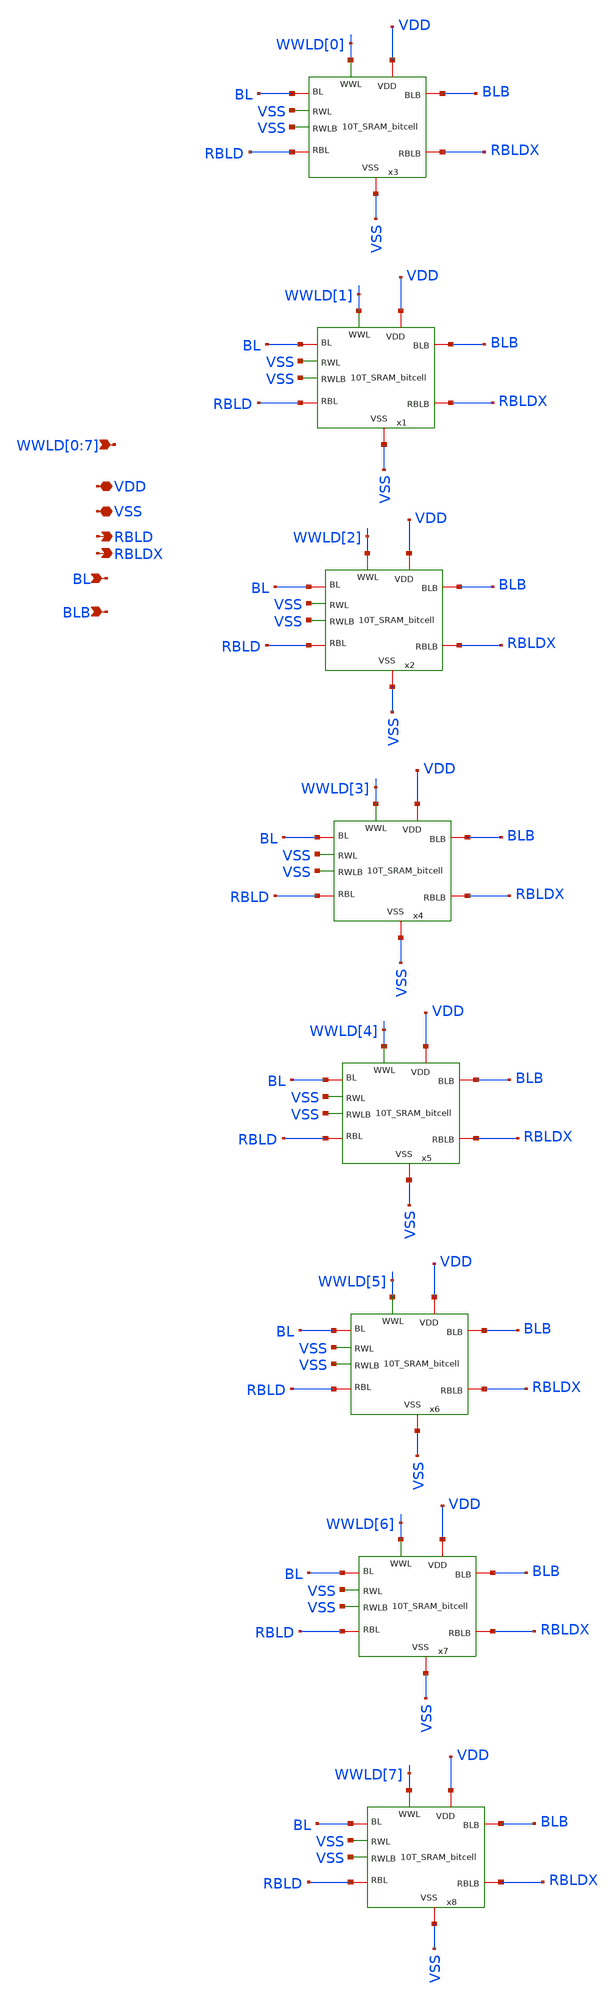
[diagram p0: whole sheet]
** sch_path: xschem/Integrated_bitcell/Dummy_SRAM.sch
**.subckt Dummy_SRAM WWLD[0],WWLD[1],WWLD[2],WWLD[3],WWLD[4],WWLD[5],WWLD[6],WWLD[7] VDD VSS RBLDX
*+ BL BLB RBLD
*.ipin WWLD[0],WWLD[1],WWLD[2],WWLD[3],WWLD[4],WWLD[5],WWLD[6],WWLD[7]
*.iopin VDD
*.iopin VSS
*.opin RBLDX
*.ipin BL
*.ipin BLB
*.opin RBLD
x3 WWLD[0] BL BLB VDD VSS VSS VSS RBLD RBLDX 10T_SRAM_bitcell
x1 WWLD[1] BL BLB VDD VSS VSS VSS RBLD RBLDX 10T_SRAM_bitcell
x2 WWLD[2] BL BLB VDD VSS VSS VSS RBLD RBLDX 10T_SRAM_bitcell
x4 WWLD[3] BL BLB VDD VSS VSS VSS RBLD RBLDX 10T_SRAM_bitcell
x5 WWLD[4] BL BLB VDD VSS VSS VSS RBLD RBLDX 10T_SRAM_bitcell
x6 WWLD[5] BL BLB VDD VSS VSS VSS RBLD RBLDX 10T_SRAM_bitcell
x7 WWLD[6] BL BLB VDD VSS VSS VSS RBLD RBLDX 10T_SRAM_bitcell
x8 WWLD[7] BL BLB VDD VSS VSS VSS RBLD RBLDX 10T_SRAM_bitcell
**.ends

* expanding   symbol:  10T_SRAM_bitcell.sym # of pins=9
** sym_path: xschem/Integrated_bitcell/10T_SRAM_bitcell.sym
** sch_path: xschem/Integrated_bitcell/10T_SRAM_bitcell.sch
.subckt 10T_SRAM_bitcell WWL BL BLB VDD VSS RWL RWLB RBL RBLB
*.iopin BL
*.iopin BLB
*.iopin VDD
*.iopin VSS
*.iopin RBL
*.iopin RBLB
*.ipin WWL
*.ipin RWL
*.ipin RWLB
XM1 net1 net2 VSS VSS sky130_fd_pr__nfet_01v8 L=0.15 W=0.64 nf=1 ad='int((nf+1)/2) * W/nf * 0.29' as='int((nf+2)/2) * W/nf * 0.29'
+ pd='2*int((nf+1)/2) * (W/nf + 0.29)' ps='2*int((nf+2)/2) * (W/nf + 0.29)' nrd='0.29 / W' nrs='0.29 / W'
+ sa=0 sb=0 sd=0 mult=1 m=1
XM2 net2 net1 VSS VSS sky130_fd_pr__nfet_01v8 L=0.15 W=0.64 nf=1 ad='int((nf+1)/2) * W/nf * 0.29' as='int((nf+2)/2) * W/nf * 0.29'
+ pd='2*int((nf+1)/2) * (W/nf + 0.29)' ps='2*int((nf+2)/2) * (W/nf + 0.29)' nrd='0.29 / W' nrs='0.29 / W'
+ sa=0 sb=0 sd=0 mult=1 m=1
XM3 net2 net1 VDD VDD sky130_fd_pr__pfet_01v8 L=0.15 W=0.42 nf=1 ad='int((nf+1)/2) * W/nf * 0.29' as='int((nf+2)/2) * W/nf * 0.29'
+ pd='2*int((nf+1)/2) * (W/nf + 0.29)' ps='2*int((nf+2)/2) * (W/nf + 0.29)' nrd='0.29 / W' nrs='0.29 / W'
+ sa=0 sb=0 sd=0 mult=1 m=1
XM4 net1 net2 VDD VDD sky130_fd_pr__pfet_01v8 L=0.15 W=0.42 nf=1 ad='int((nf+1)/2) * W/nf * 0.29' as='int((nf+2)/2) * W/nf * 0.29'
+ pd='2*int((nf+1)/2) * (W/nf + 0.29)' ps='2*int((nf+2)/2) * (W/nf + 0.29)' nrd='0.29 / W' nrs='0.29 / W'
+ sa=0 sb=0 sd=0 mult=1 m=1
XM6 net1 WWL BLB VSS sky130_fd_pr__nfet_01v8 L=0.15 W=0.42 nf=1 ad='int((nf+1)/2) * W/nf * 0.29' as='int((nf+2)/2) * W/nf * 0.29'
+ pd='2*int((nf+1)/2) * (W/nf + 0.29)' ps='2*int((nf+2)/2) * (W/nf + 0.29)' nrd='0.29 / W' nrs='0.29 / W'
+ sa=0 sb=0 sd=0 mult=1 m=1
XM5 net2 WWL BL VSS sky130_fd_pr__nfet_01v8 L=0.15 W=0.42 nf=1 ad='int((nf+1)/2) * W/nf * 0.29' as='int((nf+2)/2) * W/nf * 0.29'
+ pd='2*int((nf+1)/2) * (W/nf + 0.29)' ps='2*int((nf+2)/2) * (W/nf + 0.29)' nrd='0.29 / W' nrs='0.29 / W'
+ sa=0 sb=0 sd=0 mult=1 m=1
XM7 VSS net2 net3 VSS sky130_fd_pr__nfet_01v8 L=0.15 W=0.42 nf=1 ad='int((nf+1)/2) * W/nf * 0.29' as='int((nf+2)/2) * W/nf * 0.29'
+ pd='2*int((nf+1)/2) * (W/nf + 0.29)' ps='2*int((nf+2)/2) * (W/nf + 0.29)' nrd='0.29 / W' nrs='0.29 / W'
+ sa=0 sb=0 sd=0 mult=1 m=1
XM8 RBL RWL net3 VSS sky130_fd_pr__nfet_01v8 L=0.15 W=0.42 nf=1 ad='int((nf+1)/2) * W/nf * 0.29' as='int((nf+2)/2) * W/nf * 0.29'
+ pd='2*int((nf+1)/2) * (W/nf + 0.29)' ps='2*int((nf+2)/2) * (W/nf + 0.29)' nrd='0.29 / W' nrs='0.29 / W'
+ sa=0 sb=0 sd=0 mult=1 m=1
XM9 VSS net1 net4 VSS sky130_fd_pr__nfet_01v8 L=0.15 W=0.42 nf=1 ad='int((nf+1)/2) * W/nf * 0.29' as='int((nf+2)/2) * W/nf * 0.29'
+ pd='2*int((nf+1)/2) * (W/nf + 0.29)' ps='2*int((nf+2)/2) * (W/nf + 0.29)' nrd='0.29 / W' nrs='0.29 / W'
+ sa=0 sb=0 sd=0 mult=1 m=1
XM10 RBLB RWLB net4 VSS sky130_fd_pr__nfet_01v8 L=0.15 W=0.42 nf=1 ad='int((nf+1)/2) * W/nf * 0.29' as='int((nf+2)/2) * W/nf * 0.29'
+ pd='2*int((nf+1)/2) * (W/nf + 0.29)' ps='2*int((nf+2)/2) * (W/nf + 0.29)' nrd='0.29 / W' nrs='0.29 / W'
+ sa=0 sb=0 sd=0 mult=1 m=1
.ends

.end
